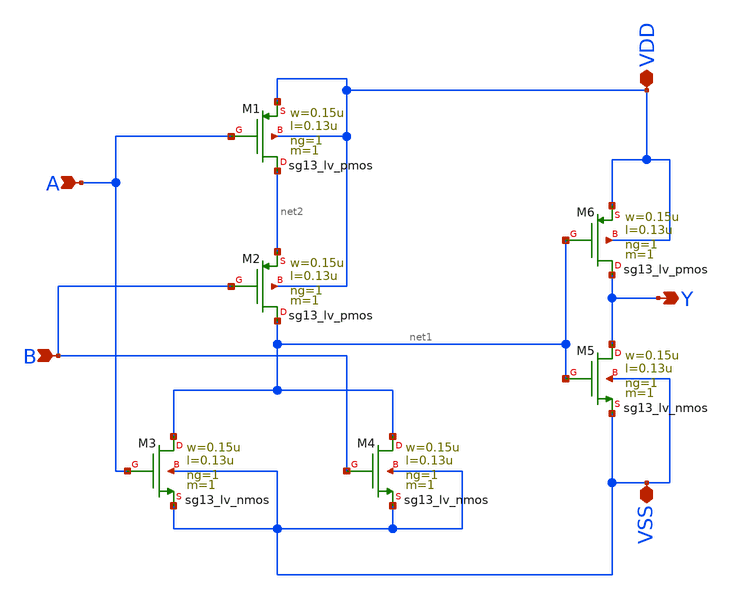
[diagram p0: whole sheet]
** sch_path: LogicGate/OR2.sch
**.subckt OR2 A B Y VDD VSS
*.ipin A
*.ipin B
*.opin Y
*.iopin VDD
*.iopin VSS
XM5 Y net1 VSS VSS sg13_lv_nmos w=0.15u l=0.13u ng=1 m=1 mm_ok=1
XM6 Y net1 VDD VDD sg13_lv_pmos w=0.15u l=0.13u ng=1 m=1 mm_ok=1
XM1 net2 A VDD VDD sg13_lv_pmos w=0.15u l=0.13u ng=1 m=1 mm_ok=1
XM2 net1 B net2 VDD sg13_lv_pmos w=0.15u l=0.13u ng=1 m=1 mm_ok=1
XM3 net1 A VSS VSS sg13_lv_nmos w=0.15u l=0.13u ng=1 m=1 mm_ok=1
XM4 net1 B VSS VSS sg13_lv_nmos w=0.15u l=0.13u ng=1 m=1 mm_ok=1
**.ends
.end
